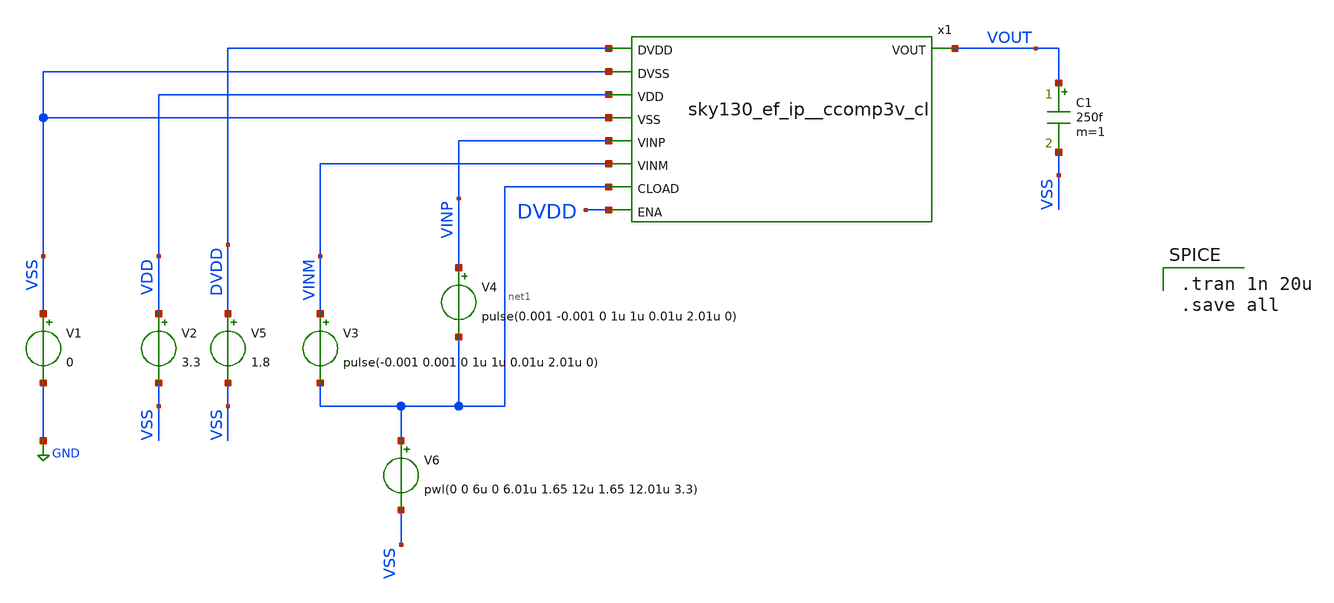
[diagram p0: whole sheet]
** sch_path: xschem/sky130_ef_ip__ccomp3v_tb.sch
**.subckt sky130_ef_ip__ccomp3v_tb
V1 VSS GND 0
V2 VDD VSS 3.3
C1 VOUT VSS 250f m=1
V3 VINM net1 pulse(-0.001 0.001 0 1u 1u 0.01u 2.01u 0)
V4 VINP net1 pulse(0.001 -0.001 0 1u 1u 0.01u 2.01u 0)
V5 DVDD VSS 1.8
V6 net1 VSS pwl(0 0 6u 0 6.01u 1.65 12u 1.65 12.01u 3.3)
x1 VOUT DVDD VSS VDD VSS VINP VINM net1 DVDD sky130_ef_ip__ccomp3v_cl
**** begin user architecture code
.lib $::SKYWATER_MODELS/sky130.lib.spice tt

.tran 1n 20u
.save all



.include /usr/share/pdk/sky130A/libs.ref/sky130_fd_sc_hvl/spice/sky130_fd_sc_hvl.spice

**** end user architecture code
**.ends
.GLOBAL GND
.end
